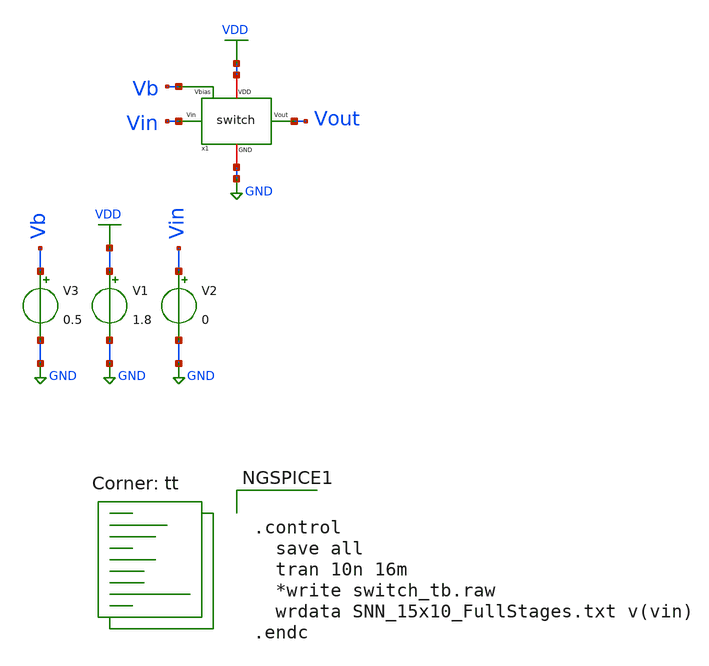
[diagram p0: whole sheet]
** sch_path: SNN/WU_Circuit_tb.sch
**.subckt WU_Circuit_tb
V1 VDD GND 1.8
V2 Vin GND 0
V3 Vb GND 0.5
x1 Vin GND VDD Vout Vb switch
**** begin user architecture code
.lib $::SKYWATER_MODELS/sky130.lib.spice tt


.control
  save all
  tran 10n 16m
  *write switch_tb.raw
  wrdata SNN_15x10_FullStages.txt v(vin)
.endc


**** end user architecture code
**.ends

* expanding   symbol:  /home/ricardo/RATT_repos/Proyectos_xschem/switch/switch.sym # of pins=5
** sym_path: switch/switch.sym
** sch_path: switch/switch.sch
.subckt switch Vin GND VDD Vout Vbias
*.iopin GND
*.iopin VDD
*.opin Vout
*.ipin Vin
*.ipin Vbias
XM1 Vout net1 Vin VDD sky130_fd_pr__pfet_01v8 L=0.15 W=0.45 nf=1 ad='int((nf+1)/2) * W/nf * 0.29' as='int((nf+2)/2) * W/nf * 0.29'
+ pd='2*int((nf+1)/2) * (W/nf + 0.29)' ps='2*int((nf+2)/2) * (W/nf + 0.29)' nrd='0.29 / W' nrs='0.29 / W'
+ sa=0 sb=0 sd=0 mult=1 m=1
XM2 Vin Vin Vout GND sky130_fd_pr__nfet_01v8 L=0.15 W=0.45 nf=1 ad='int((nf+1)/2) * W/nf * 0.29' as='int((nf+2)/2) * W/nf * 0.29'
+ pd='2*int((nf+1)/2) * (W/nf + 0.29)' ps='2*int((nf+2)/2) * (W/nf + 0.29)' nrd='0.29 / W' nrs='0.29 / W'
+ sa=0 sb=0 sd=0 mult=1 m=1
XM3 net1 Vin VDD VDD sky130_fd_pr__pfet_01v8 L=0.15 W=0.45 nf=1 ad='int((nf+1)/2) * W/nf * 0.29' as='int((nf+2)/2) * W/nf * 0.29'
+ pd='2*int((nf+1)/2) * (W/nf + 0.29)' ps='2*int((nf+2)/2) * (W/nf + 0.29)' nrd='0.29 / W' nrs='0.29 / W'
+ sa=0 sb=0 sd=0 mult=1 m=1
XM4 net1 Vin GND GND sky130_fd_pr__nfet_01v8 L=0.15 W=0.45 nf=1 ad='int((nf+1)/2) * W/nf * 0.29' as='int((nf+2)/2) * W/nf * 0.29'
+ pd='2*int((nf+1)/2) * (W/nf + 0.29)' ps='2*int((nf+2)/2) * (W/nf + 0.29)' nrd='0.29 / W' nrs='0.29 / W'
+ sa=0 sb=0 sd=0 mult=1 m=1
XM5 Vout Vbias GND GND sky130_fd_pr__nfet_01v8 L=0.15 W=0.45 nf=1 ad='int((nf+1)/2) * W/nf * 0.29' as='int((nf+2)/2) * W/nf * 0.29'
+ pd='2*int((nf+1)/2) * (W/nf + 0.29)' ps='2*int((nf+2)/2) * (W/nf + 0.29)' nrd='0.29 / W' nrs='0.29 / W'
+ sa=0 sb=0 sd=0 mult=1 m=1
.ends

.GLOBAL GND
.GLOBAL VDD
.end
